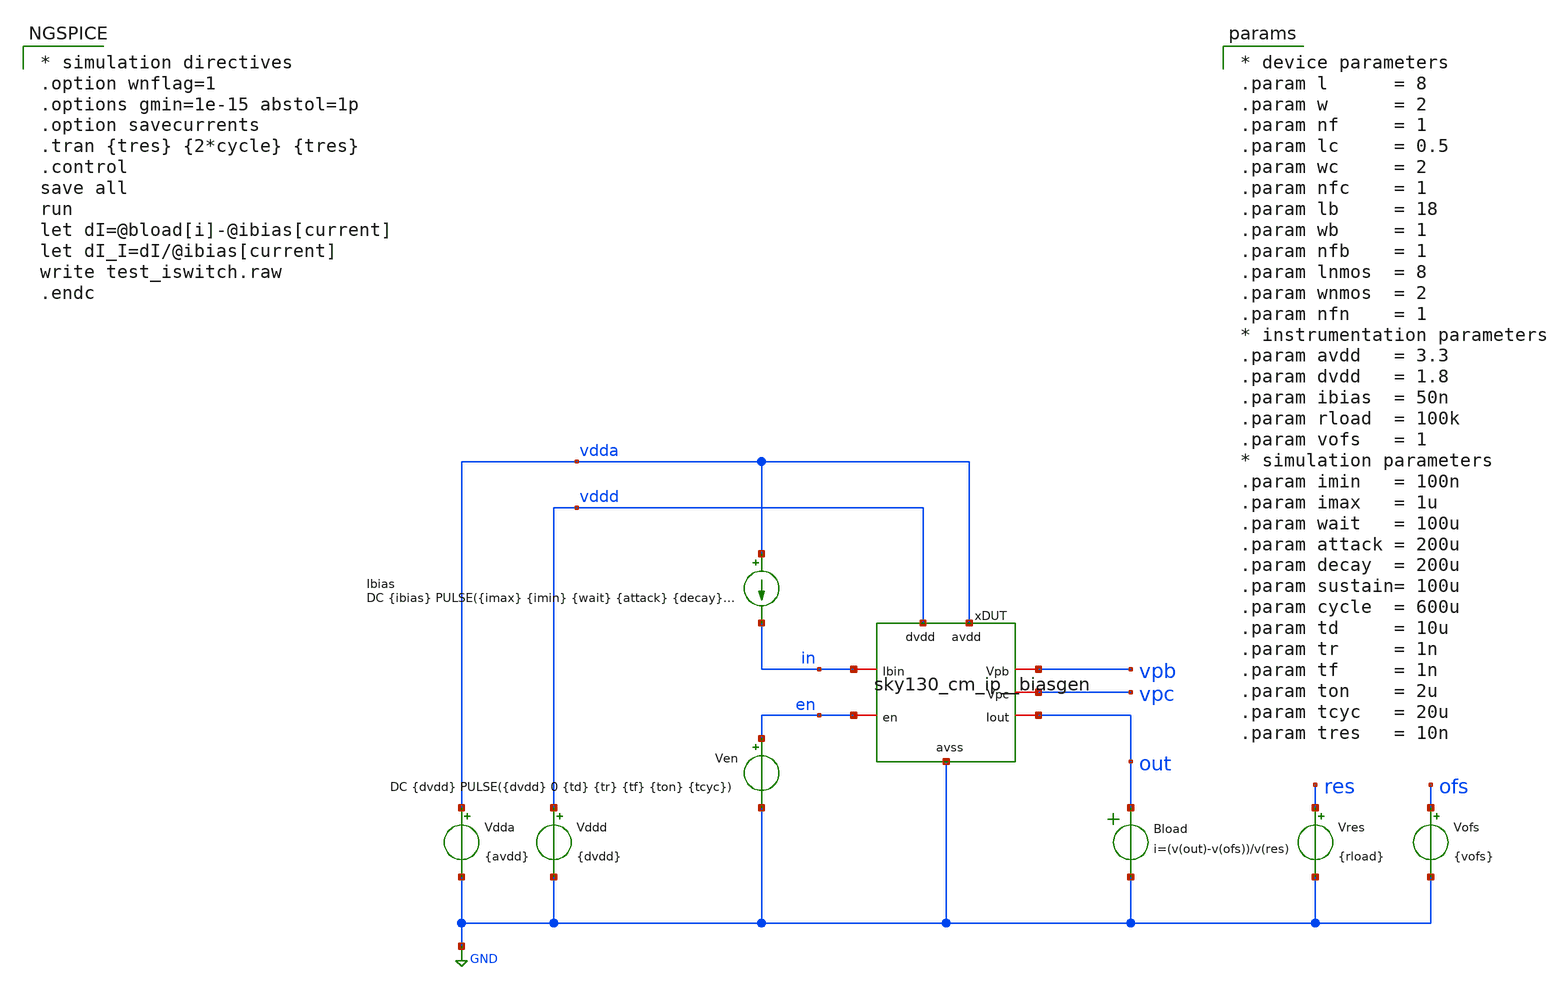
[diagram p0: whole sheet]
** sch_path: xschem/test_iswitch.sch
**.subckt test_iswitch
Vdda vdda GND {avdd}
.save i(vdda)
Ibias vdda in DC {ibias} PULSE({imax} {imin} {wait} {attack} {decay} {sustain} {cycle})
Vres res GND {rload}
Bload out GND i=(v(out)-v(ofs))/v(res)
Vofs ofs GND {vofs}
xDUT vdda vpb vpc out in GND en vddd sky130_cm_ip__biasgen l=8 w=2 nf=1 lc=0.5 wc=2 nfc=1 lb=18 wb=1
+ nfb=1 ln=8 wn=2 nfn=1
Vddd vddd GND {dvdd}
.save i(vddd)
Ven en GND DC {dvdd} PULSE({dvdd} 0 {td} {tr} {tf} {ton} {tcyc})
.save i(ven)
**** begin user architecture code

* device parameters
.param l      = 8
.param w      = 2
.param nf     = 1
.param lc     = 0.5
.param wc     = 2
.param nfc    = 1
.param lb     = 18
.param wb     = 1
.param nfb    = 1
.param lnmos  = 8
.param wnmos  = 2
.param nfn    = 1
* instrumentation parameters
.param avdd   = 3.3
.param dvdd   = 1.8
.param ibias  = 50n
.param rload  = 100k
.param vofs   = 1
* simulation parameters
.param imin   = 100n
.param imax   = 1u
.param wait   = 100u
.param attack = 200u
.param decay  = 200u
.param sustain= 100u
.param cycle  = 600u
.param td     = 10u
.param tr     = 1n
.param tf     = 1n
.param ton    = 2u
.param tcyc   = 20u
.param tres   = 10n


** opencircuitdesign pdks install
.lib $::SKYWATER_MODELS/sky130.lib.spice tt



* simulation directives
.option wnflag=1
.options gmin=1e-15 abstol=1p
.option savecurrents
.tran {tres} {2*cycle} {tres}
.control
save all
run
let dI=@bload[i]-@ibias[current]
let dI_I=dI/@ibias[current]
write test_iswitch.raw
.endc


**** end user architecture code
**.ends

* expanding   symbol:  xschem/sky130_cm_ip__biasgen.sym # of pins=8
** sym_path: xschem/sky130_cm_ip__biasgen.sym
** sch_path: xschem/sky130_cm_ip__biasgen.sch
.subckt sky130_cm_ip__biasgen avdd Vpb Vpc Iout Ibin avss en dvdd  l=8 w=2 nf=1 lc=0.5 wc=2 nfc=1
+ lb=18 wb=1 nfb=1 lnmos=8 wnmos=2 nfnmos=1
*.iopin avss
*.iopin avdd
*.iopin Ibin
*.iopin Vpb
*.iopin Vpc
*.iopin Iout
*.iopin dvdd
*.iopin en
XMc3 Vpc Vpc avdd avdd sky130_fd_pr__pfet_g5v0d10v5 L={lb} W={wb} nf={nfb} ad='int(({nfb} + 1)/2) * {wb} / {nfb} * 0.29'
+ as='int(({nfb} + 2)/2) * {wb} / {nfb} * 0.29' pd='2*int(({nfb} + 1)/2) * ({wb} / {nfb} + 0.29)' ps='2*int(({nfb} + 2)/2) * ({wb} / {nfb} + 0.29)'
+ nrd='0.29 / {wb} ' nrs='0.29 / {wb} ' sa=0 sb=0 sd=0 mult=1 m=1
XMn1 Ibin Ibin avss avss sky130_fd_pr__nfet_g5v0d10v5 L={lnmos} W={wnmos} nf={nfnmos} ad='int(({nfnmos} + 1)/2) * {wnmos} / {nfnmos} * 0.29'
+ as='int(({nfnmos} + 2)/2) * {wnmos} / {nfnmos} * 0.29' pd='2*int(({nfnmos} + 1)/2) * ({wnmos} / {nfnmos} + 0.29)'
+ ps='2*int(({nfnmos} + 2)/2) * ({wnmos} / {nfnmos} + 0.29)' nrd='0.29 / {wnmos} ' nrs='0.29 / {wnmos} '
+ sa=0 sb=0 sd=0 mult=1 m=1
XMn2 Vpc Ibin avss avss sky130_fd_pr__nfet_g5v0d10v5 L={lnmos} W={wnmos} nf={nfnmos} ad='int(({nfnmos} + 1)/2) * {wnmos} / {nfnmos} * 0.29'
+ as='int(({nfnmos} + 2)/2) * {wnmos} / {nfnmos} * 0.29' pd='2*int(({nfnmos} + 1)/2) * ({wnmos} / {nfnmos} + 0.29)'
+ ps='2*int(({nfnmos} + 2)/2) * ({wnmos} / {nfnmos} + 0.29)' nrd='0.29 / {wnmos} ' nrs='0.29 / {wnmos} '
+ sa=0 sb=0 sd=0 mult=1 m=1
XMn3 Vpb Ibin avss avss sky130_fd_pr__nfet_g5v0d10v5 L={lnmos} W={wnmos} nf={nfnmos} ad='int(({nfnmos} + 1)/2) * {wnmos} / {nfnmos} * 0.29'
+ as='int(({nfnmos} + 2)/2) * {wnmos} / {nfnmos} * 0.29' pd='2*int(({nfnmos} + 1)/2) * ({wnmos} / {nfnmos} + 0.29)'
+ ps='2*int(({nfnmos} + 2)/2) * ({wnmos} / {nfnmos} + 0.29)' nrd='0.29 / {wnmos} ' nrs='0.29 / {wnmos} '
+ sa=0 sb=0 sd=0 mult=1 m=1
xlvl avdd vgoff dvdd vgon en avss sky130_cm_levelshifter
x0 avdd avdd Vpb avss Vpc Vpb sky130_cm_sw_psource l={l} w={w} nf={nf} lc={lc} wc={wc} nfc={nfc} lon=.5
+ won=1 nfon=1 loff=.5 woff=1 nfoff=1
x1 avdd vgoff Vpb vgon Vpc Iout sky130_cm_sw_psource l={l} w={w} nf={nf} lc={lc} wc={wc} nfc={nfc} lon=.5
+ won=1 nfon=1 loff=.5 woff=1 nfoff=1
.ends


* expanding   symbol:  xschem/sky130_cm_levelshifter.sym # of pins=6
** sym_path: xschem/sky130_cm_levelshifter.sym
** sch_path: xschem/sky130_cm_levelshifter.sch
.subckt sky130_cm_levelshifter avdd Q dvdd Qb A avss
*.iopin avss
*.iopin avdd
*.iopin A
*.iopin dvdd
*.iopin Qb
*.iopin Q
XMnl1 Q ab avss avss sky130_fd_pr__nfet_g5v0d10v5 L=0.5 W=6 nf=1 ad='int((1 + 1)/2) * 6 / 1 * 0.29' as='int((1 + 2)/2) * 6 / 1 * 0.29'
+ pd='2*int((1 + 1)/2) * (6 / 1 + 0.29)' ps='2*int((1 + 2)/2) * (6 / 1 + 0.29)' nrd='0.29 / 6 ' nrs='0.29 / 6 '
+ sa=0 sb=0 sd=0 mult=1 m=1
XMnl2 Qb abb avss avss sky130_fd_pr__nfet_g5v0d10v5 L=0.5 W=6 nf=1 ad='int((1 + 1)/2) * 6 / 1 * 0.29'
+ as='int((1 + 2)/2) * 6 / 1 * 0.29' pd='2*int((1 + 1)/2) * (6 / 1 + 0.29)' ps='2*int((1 + 2)/2) * (6 / 1 + 0.29)'
+ nrd='0.29 / 6 ' nrs='0.29 / 6 ' sa=0 sb=0 sd=0 mult=1 m=1
XMpl1 Q Qb avdd avdd sky130_fd_pr__pfet_g5v0d10v5 L=0.5 W=2 nf=1 ad='int((1 + 1)/2) * 2 / 1 * 0.29' as='int((1 + 2)/2) * 2 / 1 * 0.29'
+ pd='2*int((1 + 1)/2) * (2 / 1 + 0.29)' ps='2*int((1 + 2)/2) * (2 / 1 + 0.29)' nrd='0.29 / 2 ' nrs='0.29 / 2 '
+ sa=0 sb=0 sd=0 mult=1 m=1
XMpl2 Qb Q avdd avdd sky130_fd_pr__pfet_g5v0d10v5 L=0.5 W=2 nf=1 ad='int((1 + 1)/2) * 2 / 1 * 0.29' as='int((1 + 2)/2) * 2 / 1 * 0.29'
+ pd='2*int((1 + 1)/2) * (2 / 1 + 0.29)' ps='2*int((1 + 2)/2) * (2 / 1 + 0.29)' nrd='0.29 / 2 ' nrs='0.29 / 2 '
+ sa=0 sb=0 sd=0 mult=1 m=1
XMn1 ab A avss avss sky130_fd_pr__nfet_01v8 L=0.15 W=1 nf=1 ad='int((1 + 1)/2) * 1 / 1 * 0.29' as='int((1 + 2)/2) * 1 / 1 * 0.29'
+ pd='2*int((1 + 1)/2) * (1 / 1 + 0.29)' ps='2*int((1 + 2)/2) * (1 / 1 + 0.29)' nrd='0.29 / 1 ' nrs='0.29 / 1 '
+ sa=0 sb=0 sd=0 mult=1 m=1
XMp1 ab A dvdd dvdd sky130_fd_pr__pfet_01v8 L=0.15 W=2 nf=1 ad='int((nf+1)/2) * W/nf * 0.29' as='int((nf+2)/2) * W/nf * 0.29'
+ pd='2*int((nf+1)/2) * (W/nf + 0.29)' ps='2*int((nf+2)/2) * (W/nf + 0.29)' nrd='0.29 / W' nrs='0.29 / W'
+ sa=0 sb=0 sd=0 mult=1 m=1
XMn2 abb ab avss avss sky130_fd_pr__nfet_01v8 L=0.15 W=1 nf=1 ad='int((1 + 1)/2) * 1 / 1 * 0.29' as='int((1 + 2)/2) * 1 / 1 * 0.29'
+ pd='2*int((1 + 1)/2) * (1 / 1 + 0.29)' ps='2*int((1 + 2)/2) * (1 / 1 + 0.29)' nrd='0.29 / 1 ' nrs='0.29 / 1 '
+ sa=0 sb=0 sd=0 mult=1 m=1
XMp2 abb ab dvdd dvdd sky130_fd_pr__pfet_01v8 L=0.15 W=2 nf=1 ad='int((nf+1)/2) * W/nf * 0.29' as='int((nf+2)/2) * W/nf * 0.29'
+ pd='2*int((nf+1)/2) * (W/nf + 0.29)' ps='2*int((nf+2)/2) * (W/nf + 0.29)' nrd='0.29 / W' nrs='0.29 / W'
+ sa=0 sb=0 sd=0 mult=1 m=1
.ends


* expanding   symbol:  xschem/sky130_cm_sw_psource.sym # of pins=6
** sym_path: xschem/sky130_cm_sw_psource.sym
** sch_path: xschem/sky130_cm_sw_psource.sch
.subckt sky130_cm_sw_psource avdd offb Vpb onb Vpc Iout  l=8 w=2 nf=1 lc=0.5 wc=2 nfc=1 lon=.5 won=1
+ nfon=1 loff=.5 woff=1 nfoff=1
*.iopin avdd
*.iopin Vpb
*.iopin Vpc
*.iopin Iout
*.iopin offb
*.iopin onb
XMc2 Iout vsw vd avdd sky130_fd_pr__pfet_g5v0d10v5 L={lc} W={wc} nf={nfc} ad='int(({nfc} + 1)/2) * {wc} / {nfc} * 0.29'
+ as='int(({nfc} + 2)/2) * {wc} / {nfc} * 0.29' pd='2*int(({nfc} + 1)/2) * ({wc} / {nfc} + 0.29)' ps='2*int(({nfc} + 2)/2) * ({wc} / {nfc} + 0.29)'
+ nrd='0.29 / {wc} ' nrs='0.29 / {wc} ' sa=0 sb=0 sd=0 mult=1 m=1
XM2 vd Vpb avdd avdd sky130_fd_pr__pfet_g5v0d10v5 L={l} W={w} nf={nf} ad='int(({nf} + 1)/2) * {w} / {nf} * 0.29'
+ as='int(({nf} + 2)/2) * {w} / {nf} * 0.29' pd='2*int(({nf} + 1)/2) * ({w} / {nf} + 0.29)' ps='2*int(({nf} + 2)/2) * ({w} / {nf} + 0.29)'
+ nrd='0.29 / {w} ' nrs='0.29 / {w} ' sa=0 sb=0 sd=0 mult=1 m=1
XMon Vpc onb vsw avdd sky130_fd_pr__pfet_g5v0d10v5 L={lon} W={won} nf={nfon} ad='int(({nfon} + 1)/2) * {won} / {nfon} * 0.29'
+ as='int(({nfon} + 2)/2) * {won} / {nfon} * 0.29' pd='2*int(({nfon} + 1)/2) * ({won} / {nfon} + 0.29)'
+ ps='2*int(({nfon} + 2)/2) * ({won} / {nfon} + 0.29)' nrd='0.29 / {won} ' nrs='0.29 / {won} ' sa=0 sb=0
+ sd=0 mult=1 m=1
XMoff vsw offb avdd avdd sky130_fd_pr__pfet_g5v0d10v5 L={loff} W={woff} nf={nfoff} ad='int(({nfoff} + 1)/2) * {woff} / {nfoff} * 0.29'
+ as='int(({nfoff} + 2)/2) * {woff} / {nfoff} * 0.29' pd='2*int(({nfoff} + 1)/2) * ({woff} / {nfoff} + 0.29)'
+ ps='2*int(({nfoff} + 2)/2) * ({woff} / {nfoff} + 0.29)' nrd='0.29 / {woff} ' nrs='0.29 / {woff} ' sa=0
+ sb=0 sd=0 mult=1 m=1
.ends

.GLOBAL GND
.end
